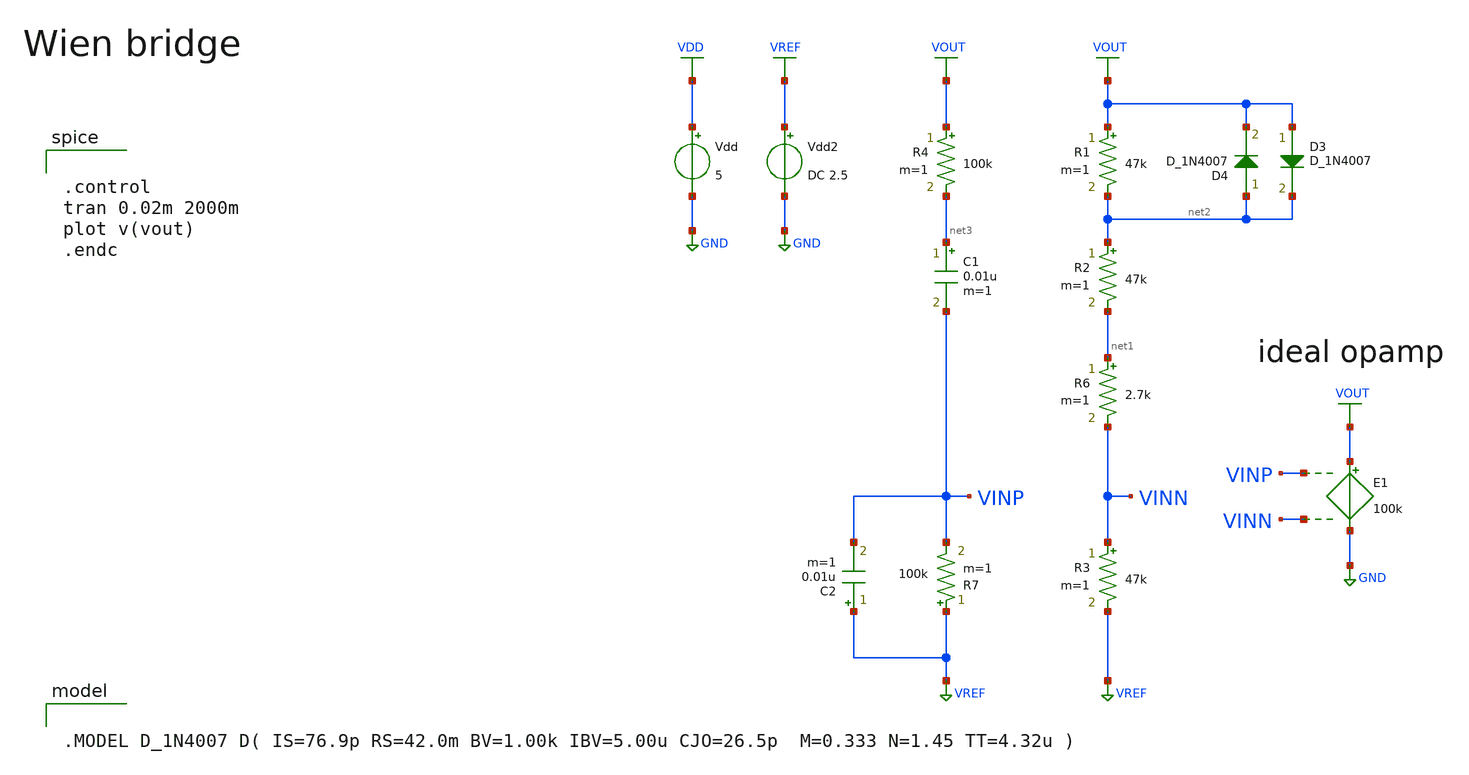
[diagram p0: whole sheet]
** sch_path: Vol.2/files/08/xschem/tb_wien_bridge_ideal.sch
**.subckt tb_wien_bridge_ideal
Vdd VDD GND 5
R1 VOUT net2 47k m=1
R2 net2 net1 47k m=1
R3 VINN VREF 47k m=1
Vdd2 VREF GND DC 2.5
R6 net1 VINN 2.7k m=1
R4 VOUT net3 100k m=1
C1 net3 VINP 0.01u m=1
R7 VREF VINP 100k m=1
C2 VREF VINP 0.01u m=1
E1 VOUT GND VINP VINN 100k
D3 VOUT net2 D_1N4007 area=1
D4 net2 VOUT D_1N4007 area=1
**** begin user architecture code


.control
tran 0.02m 2000m
plot v(vout)
.endc




.MODEL D_1N4007 D( IS=76.9p RS=42.0m BV=1.00k IBV=5.00u CJO=26.5p  M=0.333 N=1.45 TT=4.32u )


**** end user architecture code
**.ends
.GLOBAL VDD
.GLOBAL GND
.GLOBAL VOUT
.GLOBAL VREF
.end
